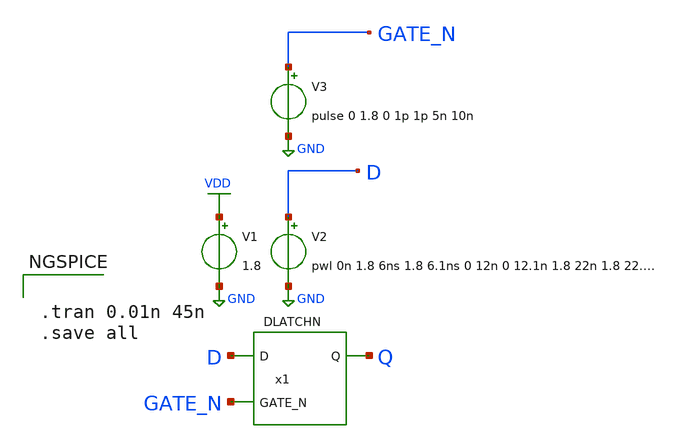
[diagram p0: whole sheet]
** sch_path: layout/xschem/sky130_rhbd/test_DLATCHN.sch
**.subckt test_DLATCHN
V2 D GND pwl 0n 1.8 6ns 1.8 6.1ns 0 12n 0 12.1n 1.8 22n 1.8 22.1n 0 27n 0 27.1n 1.8 34n 1.8 34.1n 0
V1 VDD GND 1.8
V3 GATE_N GND pulse 0 1.8 0 1p 1p 5n 10n
x1 GATE_N Q D VDD GND DLATCHN
**** begin user architecture code

.lib $::SKYWATER_MODELS/sky130.lib.spice tt


**** end user architecture code
**.ends
.GLOBAL VDD
.GLOBAL GND
**** begin user architecture code


.tran 0.01n 45n
.save all


**** end user architecture code
.end
